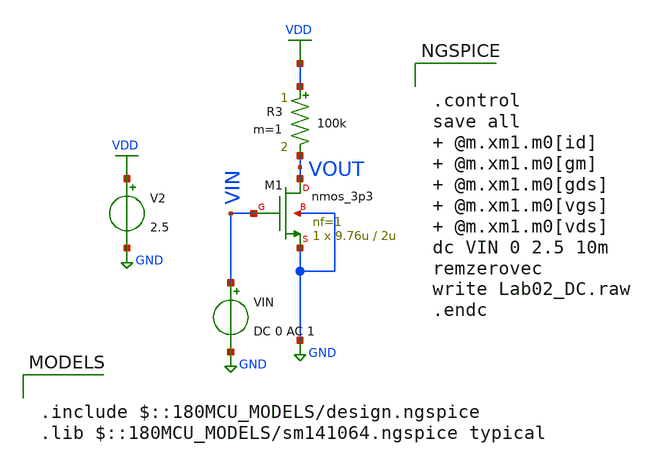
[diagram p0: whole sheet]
** sch_path: ITI_Labs/Lab2/Design/Lab02_DC.sch
**.subckt Lab02_DC
VIN VIN GND DC 0 AC 1
V2 VDD GND 2.5
R3 VDD VOUT 100k m=1
XM1 VOUT VIN GND GND nmos_3p3 L=2u W=9.76u nf=1 ad='int((nf+1)/2) * W/nf * 0.18u' as='int((nf+2)/2) * W/nf * 0.18u'
+ pd='2*int((nf+1)/2) * (W/nf + 0.18u)' ps='2*int((nf+2)/2) * (W/nf + 0.18u)' nrd='0.18u / W' nrs='0.18u / W'
+ sa=0 sb=0 sd=0 m=1
**** begin user architecture code

.include $::180MCU_MODELS/design.ngspice
.lib $::180MCU_MODELS/sm141064.ngspice typical



.control
save all  @m.xm1.m0[id]  @m.xm1.m0[gm]  @m.xm1.m0[gds]  @m.xm1.m0[vgs]  @m.xm1.m0[vds]
dc VIN 0 2.5 10m
remzerovec
write Lab02_DC.raw
.endc


**** end user architecture code
**.ends
.GLOBAL GND
.GLOBAL VDD
.end
